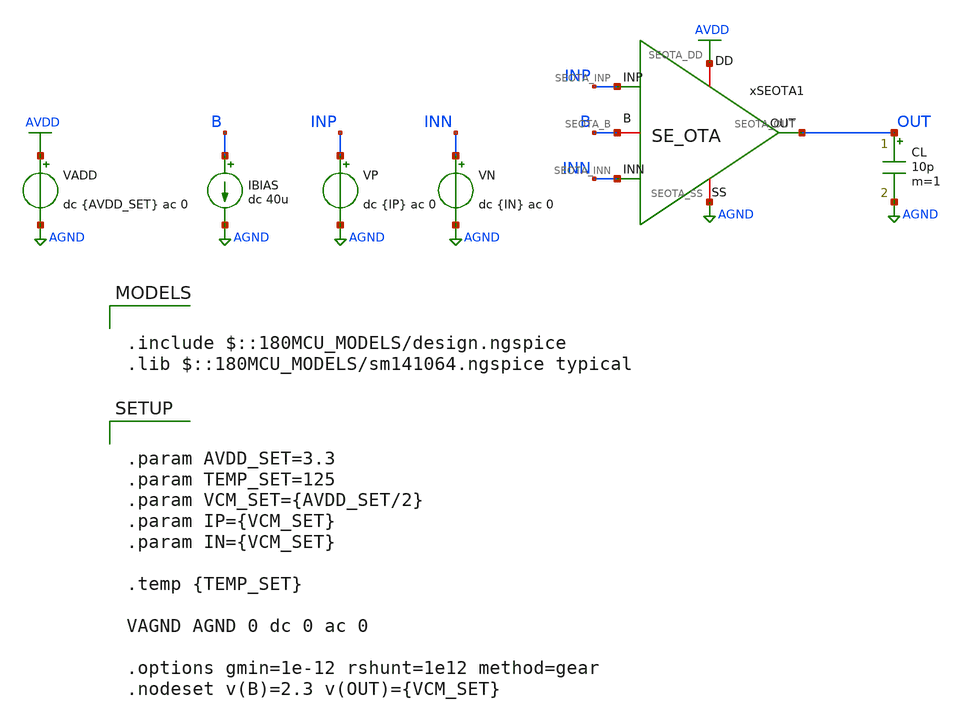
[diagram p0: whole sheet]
** sch_path: Design_Files/IC Design/Testbench/SE_OTA_OTA/Open_Loop/SE_OTA_TB_OL_C125.sch
**.subckt SE_OTA_TB_OL_C125
IBIAS B AGND dc 40u
VADD AVDD AGND dc {AVDD_SET} ac 0
.save i(vadd)
CL OUT AGND 10p m=1
VP INP AGND dc {IP} ac 0
VN INN AGND dc {IN} ac 0
xSEOTA1 AVDD AGND INP INN OUT B SE_OTA
**** begin user architecture code

.include $::180MCU_MODELS/design.ngspice
.lib $::180MCU_MODELS/sm141064.ngspice typical



.control
destroy all
save all
set wr_singlescale

shell mkdir -p /foss/designs/ECG_Acquisition_IC/Measurement_Results/IC_Simulation/SE_OTA

let avdd_run = 3.3
let vcm_run  = avdd_run/2
let off_lo   = vcm_run - 0.05
let off_hi   = vcm_run + 0.05
let off_step = 10u

* OP
op
let op_avdd  = v(AVDD)
let op_inp   = v(INP)
let op_inn   = v(INN)
let op_out   = v(OUT)
let op_b     = v(B)
let op_idd   = -vadd#branch
let op_ibias = 40e-6
wrdata /foss/designs/ECG_Acquisition_IC/Measurement_Results/IC_Simulation/SE_OTA/C125.ol_op.txt
+ op_avdd op_inp op_inn op_out op_b op_idd op_ibias

* Offset
dc VP $&off_lo $&off_hi $&off_step
wrdata /foss/designs/ECG_Acquisition_IC/Measurement_Results/IC_Simulation/SE_OTA/C125.ol_offset.txt
+ v(INP) v(INN) v(OUT)

* Diff AC
alter @VP[DC] = $&vcm_run
alter @VN[DC] = $&vcm_run
alter @VP[ACMAG] = 0.5
alter @VP[ACPHASE] = 0
alter @VN[ACMAG] = 0.5
alter @VN[ACPHASE] = 180
alter @VADD[ACMAG] = 0
alter @VAGND[ACMAG] = 0

ac dec 200 1 1G
wrdata /foss/designs/ECG_Acquisition_IC/Measurement_Results/IC_Simulation/SE_OTA/C125.ol_ac_diff.txt
+ db(v(OUT,AGND)) ph(v(OUT,AGND)) mag(v(OUT,AGND))

* CMRR
alter @VP[ACMAG] = 1
alter @VP[ACPHASE] = 0
alter @VN[ACMAG] = 1
alter @VN[ACPHASE] = 0
alter @VADD[ACMAG] = 0
alter @VAGND[ACMAG] = 0

ac dec 200 1 1G
wrdata /foss/designs/ECG_Acquisition_IC/Measurement_Results/IC_Simulation/SE_OTA/C125.ol_ac_cm.txt
+ db(v(OUT,AGND)) mag(v(OUT,AGND))

* PSRR+
alter @VP[ACMAG] = 0
alter @VN[ACMAG] = 0
alter @VADD[ACMAG] = 1
alter @VADD[ACPHASE] = 0
alter @VAGND[ACMAG] = 0

ac dec 200 1 1G
wrdata
+ /foss/designs/ECG_Acquisition_IC/Measurement_Results/IC_Simulation/SE_OTA/C125.ol_ac_psrrp.txt db(v(OUT,AGND)) mag(v(OUT,AGND))

* PSRR-
alter @VP[ACMAG] = 0
alter @VN[ACMAG] = 0
alter @VADD[ACMAG] = 0
alter @VAGND[ACMAG] = 1
alter @VAGND[ACPHASE] = 0

ac dec 200 1 1G
wrdata
+ /foss/designs/ECG_Acquisition_IC/Measurement_Results/IC_Simulation/SE_OTA/C125.ol_ac_psrrn.txt db(v(OUT,AGND)) mag(v(OUT,AGND))

* Noise total only
alter @VADD[ACMAG] = 0
alter @VAGND[ACMAG] = 0
alter @VP[ACMAG] = 1
alter @VN[ACMAG] = 0

noise v(OUT,AGND) VP dec 100 0.05 150
wrdata
+ /foss/designs/ECG_Acquisition_IC/Measurement_Results/IC_Simulation/SE_OTA/C125.ol_noise_total.txt inoise_total onoise_total

.endc




.param AVDD_SET=3.3
.param TEMP_SET=125
.param VCM_SET={AVDD_SET/2}
.param IP={VCM_SET}
.param IN={VCM_SET}

.temp {TEMP_SET}

VAGND AGND 0 dc 0 ac 0

.options gmin=1e-12 rshunt=1e12 method=gear
.nodeset v(B)=2.3 v(OUT)={VCM_SET}


**** end user architecture code
**.ends

* expanding   symbol:  ECG_Acquisition_IC/Design_Files/IC Design/Schematic/SE_OTA/SE_OTA.sym # of
*+ pins=6
** sym_path: Design_Files/IC Design/Schematic/SE_OTA/SE_OTA.sym
** sch_path: Design_Files/IC Design/Schematic/SE_OTA/SE_OTA.sch
.subckt SE_OTA SEOTA_DD SEOTA_SS SEOTA_INP SEOTA_INN SEOTA_OUT SEOTA_B
*.iopin SEOTA_DD
*.iopin SEOTA_SS
*.ipin SEOTA_INP
*.ipin SEOTA_INN
*.opin SEOTA_OUT
*.iopin SEOTA_B
XM3 net4 net4 SEOTA_DD SEOTA_DD pfet_03v3 L=4u W=1u nf=1 ad='int((nf+1)/2) * W/nf * 0.18u' as='int((nf+2)/2) * W/nf * 0.18u'
+ pd='2*int((nf+1)/2) * (W/nf + 0.18u)' ps='2*int((nf+2)/2) * (W/nf + 0.18u)' nrd='0.18u / W' nrs='0.18u / W'
+ sa=0 sb=0 sd=0 m=60
XM7 SEOTA_OUT SEOTA_B SEOTA_SS SEOTA_SS nfet_03v3 L=0.5u W=1u nf=1 ad='int((nf+1)/2) * W/nf * 0.18u'
+ as='int((nf+2)/2) * W/nf * 0.18u' pd='2*int((nf+1)/2) * (W/nf + 0.18u)' ps='2*int((nf+2)/2) * (W/nf + 0.18u)'
+ nrd='0.18u / W' nrs='0.18u / W' sa=0 sb=0 sd=0 m=100
Rz net1 net2 3.8k m=1
XM5 net3 SEOTA_B SEOTA_SS SEOTA_SS nfet_03v3 L=2u W=1u nf=1 ad='int((nf+1)/2) * W/nf * 0.18u' as='int((nf+2)/2) * W/nf * 0.18u'
+ pd='2*int((nf+1)/2) * (W/nf + 0.18u)' ps='2*int((nf+2)/2) * (W/nf + 0.18u)' nrd='0.18u / W' nrs='0.18u / W'
+ sa=0 sb=0 sd=0 m=10
XM6 SEOTA_OUT net1 SEOTA_DD SEOTA_DD pfet_03v3 L=0.5u W=1u nf=1 ad='int((nf+1)/2) * W/nf * 0.18u' as='int((nf+2)/2) * W/nf * 0.18u'
+ pd='2*int((nf+1)/2) * (W/nf + 0.18u)' ps='2*int((nf+2)/2) * (W/nf + 0.18u)' nrd='0.18u / W' nrs='0.18u / W'
+ sa=0 sb=0 sd=0 m=400
XM8 SEOTA_B SEOTA_B SEOTA_SS SEOTA_SS nfet_03v3 L=2u W=1u nf=1 ad='int((nf+1)/2) * W/nf * 0.18u' as='int((nf+2)/2) * W/nf * 0.18u'
+ pd='2*int((nf+1)/2) * (W/nf + 0.18u)' ps='2*int((nf+2)/2) * (W/nf + 0.18u)' nrd='0.18u / W' nrs='0.18u / W'
+ sa=0 sb=0 sd=0 m=20
Cc net2 SEOTA_OUT 2p m=1
XM4 net1 net4 SEOTA_DD SEOTA_DD pfet_03v3 L=4u W=1u nf=1 ad='int((nf+1)/2) * W/nf * 0.18u' as='int((nf+2)/2) * W/nf * 0.18u'
+ pd='2*int((nf+1)/2) * (W/nf + 0.18u)' ps='2*int((nf+2)/2) * (W/nf + 0.18u)' nrd='0.18u / W' nrs='0.18u / W'
+ sa=0 sb=0 sd=0 m=60
XM1 net4 SEOTA_INN net3 SEOTA_SS nfet_03v3 L=4u W=1u nf=1 ad='int((nf+1)/2) * W/nf * 0.18u' as='int((nf+2)/2) * W/nf * 0.18u'
+ pd='2*int((nf+1)/2) * (W/nf + 0.18u)' ps='2*int((nf+2)/2) * (W/nf + 0.18u)' nrd='0.18u / W' nrs='0.18u / W'
+ sa=0 sb=0 sd=0 m=400
XM2 net1 SEOTA_INP net3 SEOTA_SS nfet_03v3 L=4u W=1u nf=1 ad='int((nf+1)/2) * W/nf * 0.18u' as='int((nf+2)/2) * W/nf * 0.18u'
+ pd='2*int((nf+1)/2) * (W/nf + 0.18u)' ps='2*int((nf+2)/2) * (W/nf + 0.18u)' nrd='0.18u / W' nrs='0.18u / W'
+ sa=0 sb=0 sd=0 m=400
.ends

.GLOBAL AVDD
.GLOBAL AGND
.end
